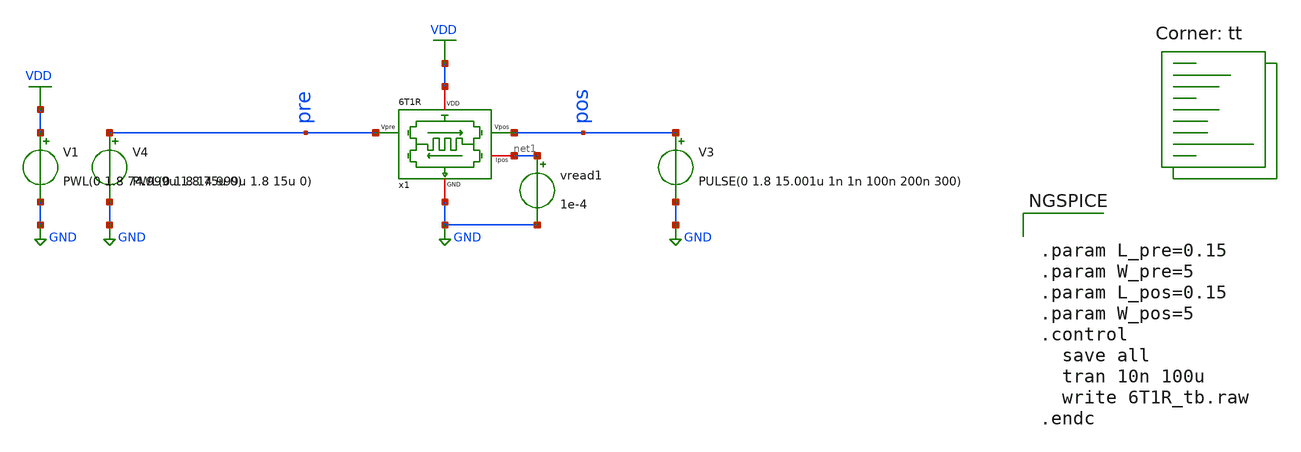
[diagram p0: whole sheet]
** sch_path: synapse/6T1R_tb.sch
**.subckt 6T1R_tb
V1 VDD GND PWL(0 1.8 74.999u 1.8 75u 0)
V3 pos GND PULSE(0 1.8 15.001u 1n 1n 100n 200n 300)
vread1 net1 GND 1e-4
x1 VDD net1 pre pos GND 6T1R
V4 pre GND PWL(0 1.8 14.999u 1.8 15u 0)
**** begin user architecture code
.lib $::SKYWATER_MODELS/sky130.lib.spice tt

** opencircuitdesign pdks install
.inc $::SKYWATER_MODELS/rram_v0.spice



.param L_pre=0.15
.param W_pre=5
.param L_pos=0.15
.param W_pos=5
.control
  save all
  tran 10n 100u
  write 6T1R_tb.raw
.endc


**** end user architecture code
**.ends

* expanding   symbol:  /home/ricardo/RATT_repos/Proyectos_xschem/synapse/6T1R.sym # of pins=5
** sym_path: synapse/6T1R.sym
** sch_path: synapse/6T1R.sch
.subckt 6T1R VDD Ipos Vpre Vpos GND
*.ipin Vpre
*.ipin Vpos
*.iopin GND
*.iopin Ipos
*.iopin VDD
XM1 vipre Vpre net1 GND sky130_fd_pr__nfet_01v8 L={L_pre} W={W_pre} nf=1 ad='int((nf+1)/2) * W/nf * 0.29'
+ as='int((nf+2)/2) * W/nf * 0.29' pd='2*int((nf+1)/2) * (W/nf + 0.29)' ps='2*int((nf+2)/2) * (W/nf + 0.29)'
+ nrd='0.29 / W' nrs='0.29 / W' sa=0 sb=0 sd=0 mult=1 m=1
XR1 net2 net1 rram_v0
XM3 vipre Vpos net2 GND sky130_fd_pr__nfet_01v8 L={L_pos} W={W_pos} nf=1 ad='int((nf+1)/2) * W/nf * 0.29'
+ as='int((nf+2)/2) * W/nf * 0.29' pd='2*int((nf+1)/2) * (W/nf + 0.29)' ps='2*int((nf+2)/2) * (W/nf + 0.29)'
+ nrd='0.29 / W' nrs='0.29 / W' sa=0 sb=0 sd=0 mult=1 m=1
XM6 Ipos vipre VDD VDD sky130_fd_pr__pfet_01v8 L=0.15 W=1.5 nf=1 ad='int((nf+1)/2) * W/nf * 0.29' as='int((nf+2)/2) * W/nf * 0.29'
+ pd='2*int((nf+1)/2) * (W/nf + 0.29)' ps='2*int((nf+2)/2) * (W/nf + 0.29)' nrd='0.29 / W' nrs='0.29 / W'
+ sa=0 sb=0 sd=0 mult=1 m=1
XM5 vipre vipre VDD VDD sky130_fd_pr__pfet_01v8 L=0.15 W=10 nf=1 ad='int((nf+1)/2) * W/nf * 0.29' as='int((nf+2)/2) * W/nf * 0.29'
+ pd='2*int((nf+1)/2) * (W/nf + 0.29)' ps='2*int((nf+2)/2) * (W/nf + 0.29)' nrd='0.29 / W' nrs='0.29 / W'
+ sa=0 sb=0 sd=0 mult=1 m=1
XM2 net1 Vpos GND GND sky130_fd_pr__nfet_01v8 L={L_pos} W={W_pos} nf=1 ad='int((nf+1)/2) * W/nf * 0.29'
+ as='int((nf+2)/2) * W/nf * 0.29' pd='2*int((nf+1)/2) * (W/nf + 0.29)' ps='2*int((nf+2)/2) * (W/nf + 0.29)'
+ nrd='0.29 / W' nrs='0.29 / W' sa=0 sb=0 sd=0 mult=1 m=1
XM4 net2 Vpre GND GND sky130_fd_pr__nfet_01v8 L={L_pre} W={W_pre} nf=1 ad='int((nf+1)/2) * W/nf * 0.29'
+ as='int((nf+2)/2) * W/nf * 0.29' pd='2*int((nf+1)/2) * (W/nf + 0.29)' ps='2*int((nf+2)/2) * (W/nf + 0.29)'
+ nrd='0.29 / W' nrs='0.29 / W' sa=0 sb=0 sd=0 mult=1 m=1
.ends

.GLOBAL GND
.GLOBAL VDD
.end
